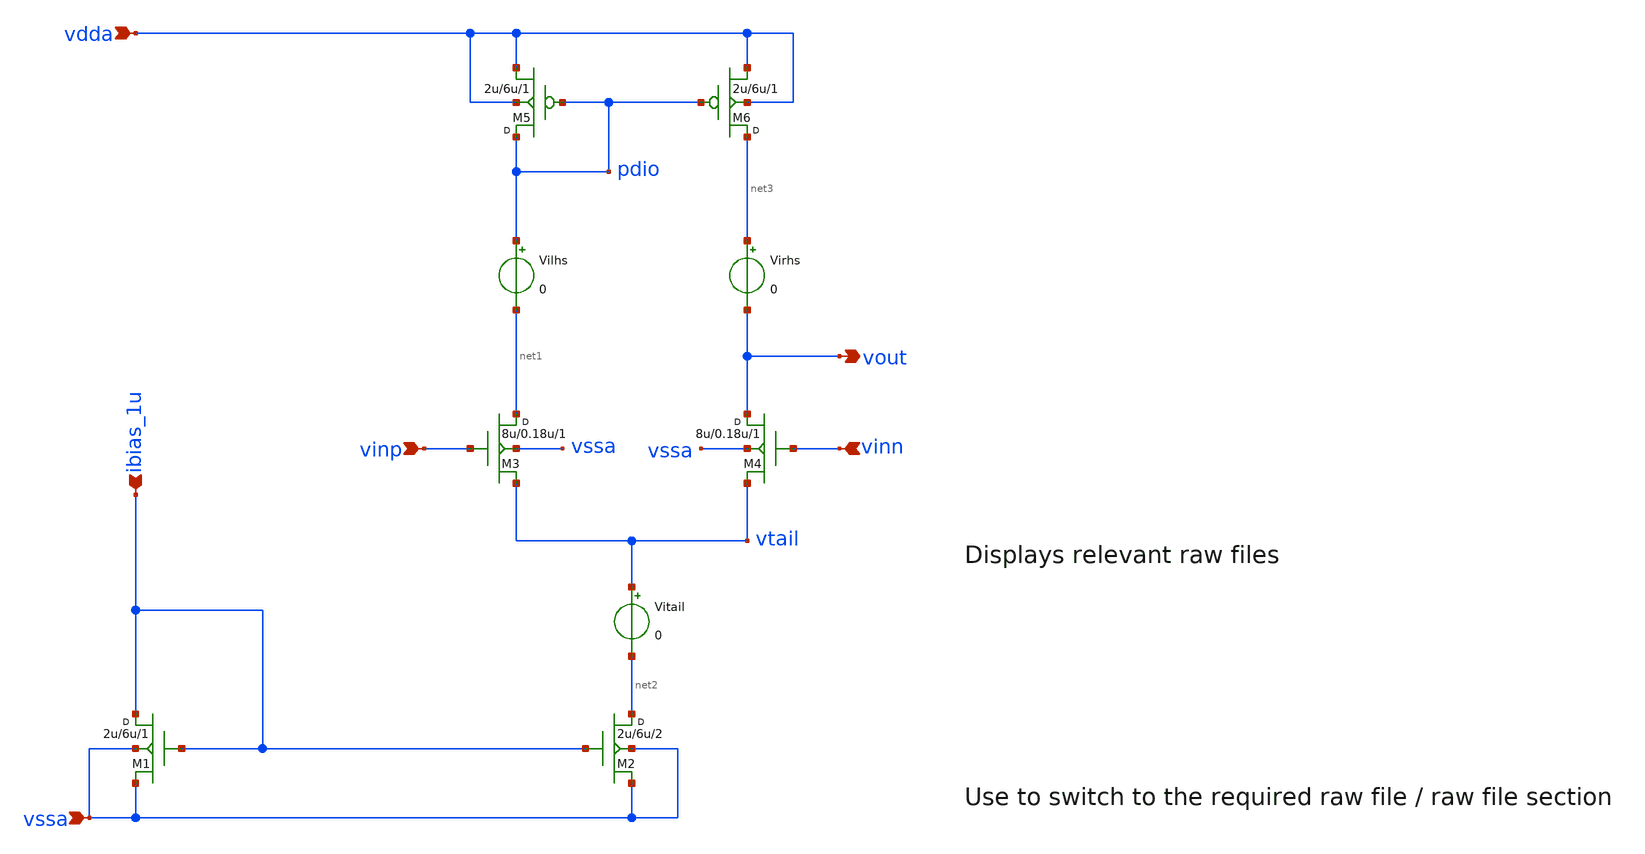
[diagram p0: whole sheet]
** sch_path: Analysing_DCOPs_in_ngspice_xschem/OTA_DCOP.sch
**.subckt OTA_DCOP vdda vssa ibias_1u vinn vinp vout
*.ipin vdda
*.ipin vssa
*.ipin ibias_1u
*.ipin vinn
*.ipin vinp
*.opin vout
M6 net3 pdio vdda vdda pmosx w=2u l=6u m=1
M5 pdio pdio vdda vdda pmosx w=2u l=6u m=1
M3 net1 vinp vtail vssa nmos w=8u l=0.18u m=1
M4 vout vinn vtail vssa nmos w=8u l=0.18u m=1
M2 net2 ibias_1u vssa vssa nmos w=2u l=6u m=2
M1 ibias_1u ibias_1u vssa vssa nmos w=2u l=6u m=1
Vilhs pdio net1 0
Virhs net3 vout 0
Vitail vtail net2 0
**.ends
.end
